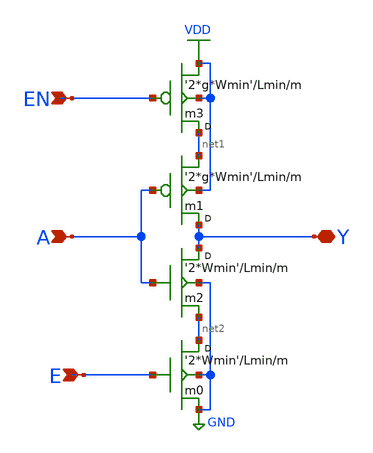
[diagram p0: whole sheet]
** sch_path: Sources/crafted/tri.sch
**.subckt tri A Y EN E
*.ipin A
*.iopin Y
*.ipin EN
*.ipin E
m2 Y A net2 GND nmos4 w='2*Wmin' l=Lmin m=m
m1 Y A net1 VDD pmos4 w='2*g*Wmin' l=Lmin m=m
m0 net2 E GND GND nmos4 w='2*Wmin' l=Lmin m=m
m3 net1 EN VDD VDD pmos4 w='2*g*Wmin' l=Lmin m=m
**.ends
.GLOBAL VDD
.GLOBAL GND
.end
